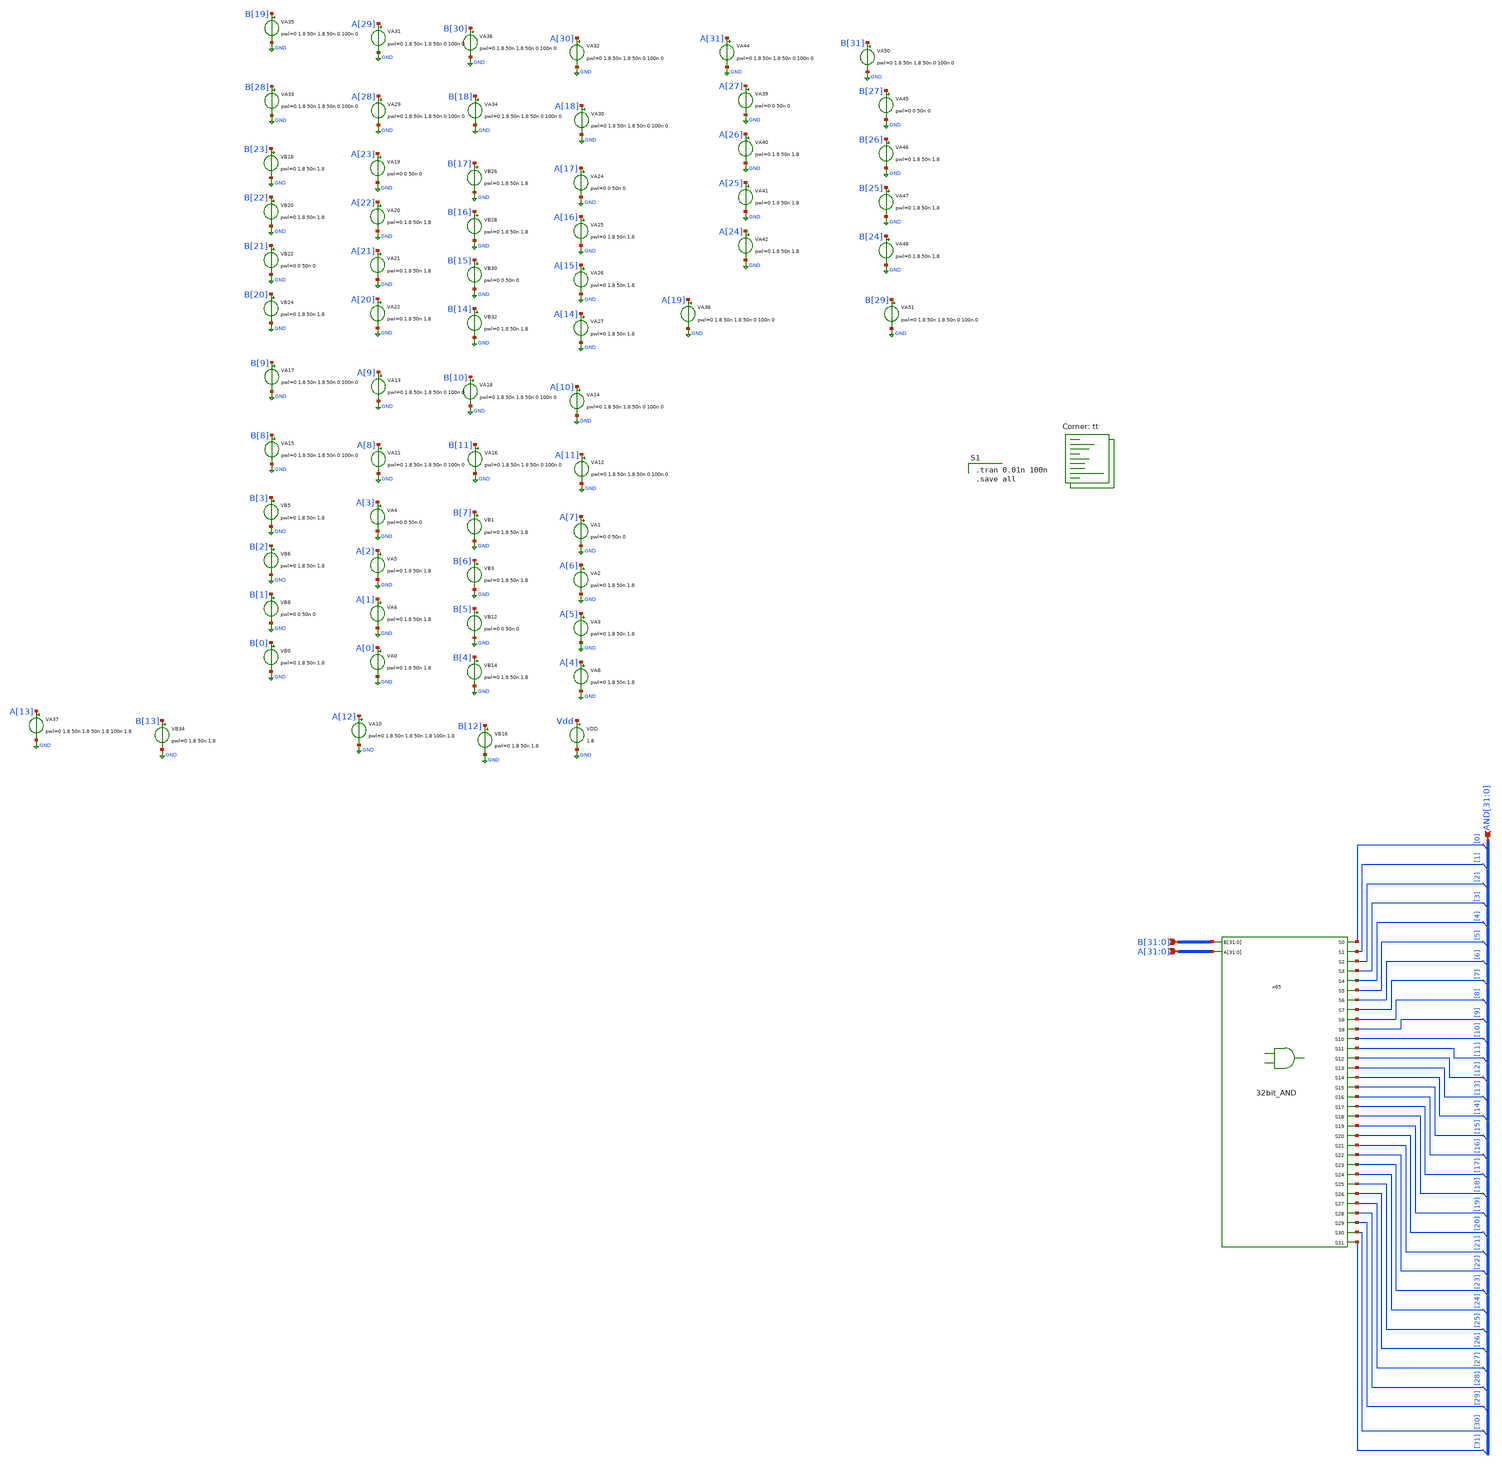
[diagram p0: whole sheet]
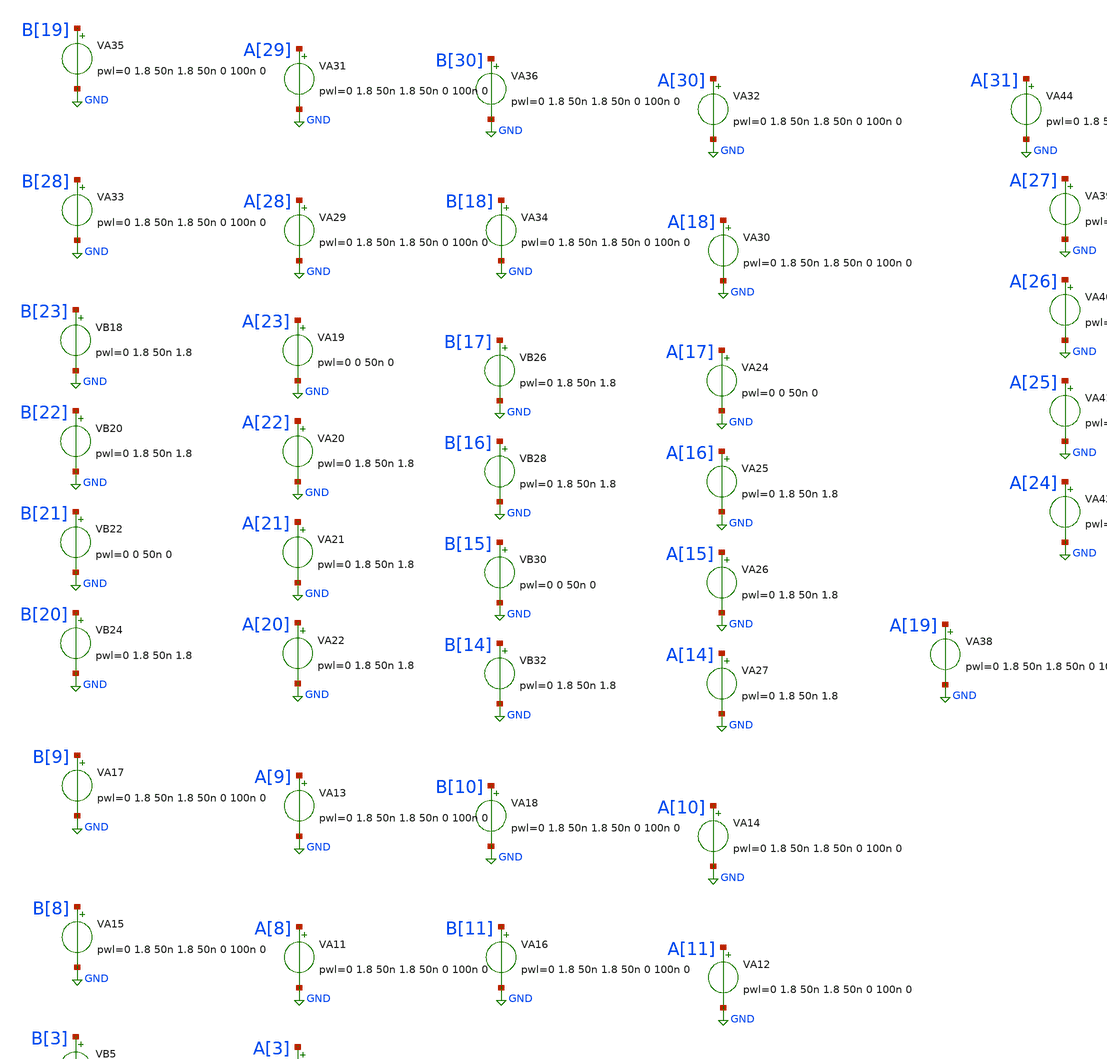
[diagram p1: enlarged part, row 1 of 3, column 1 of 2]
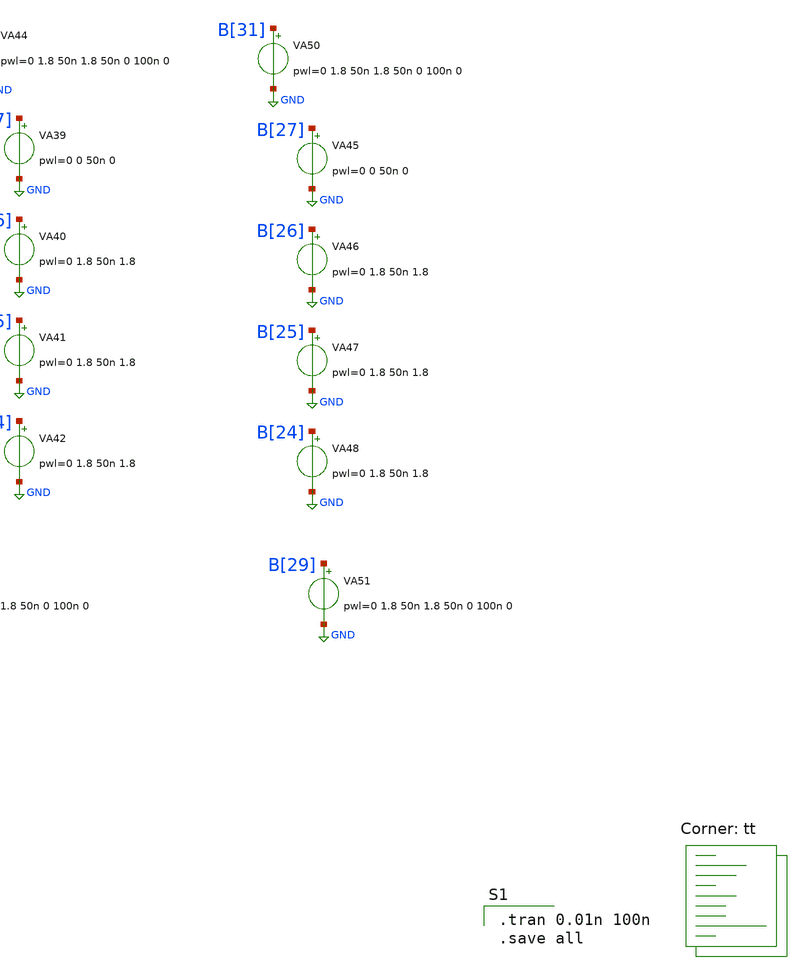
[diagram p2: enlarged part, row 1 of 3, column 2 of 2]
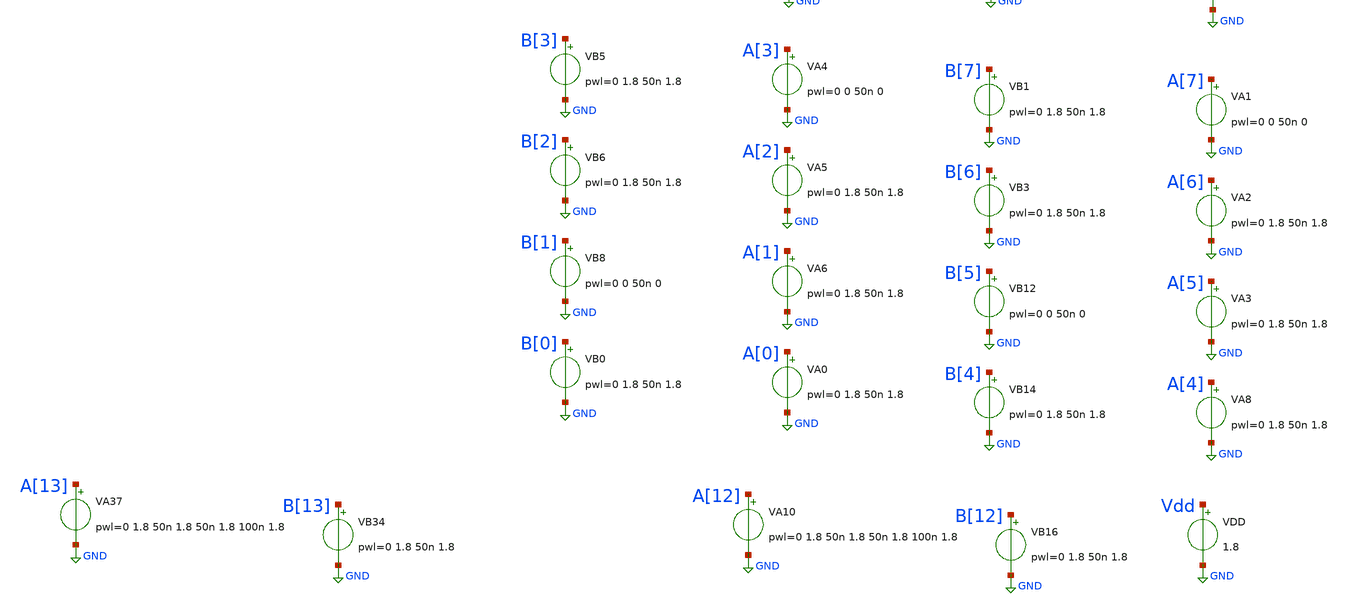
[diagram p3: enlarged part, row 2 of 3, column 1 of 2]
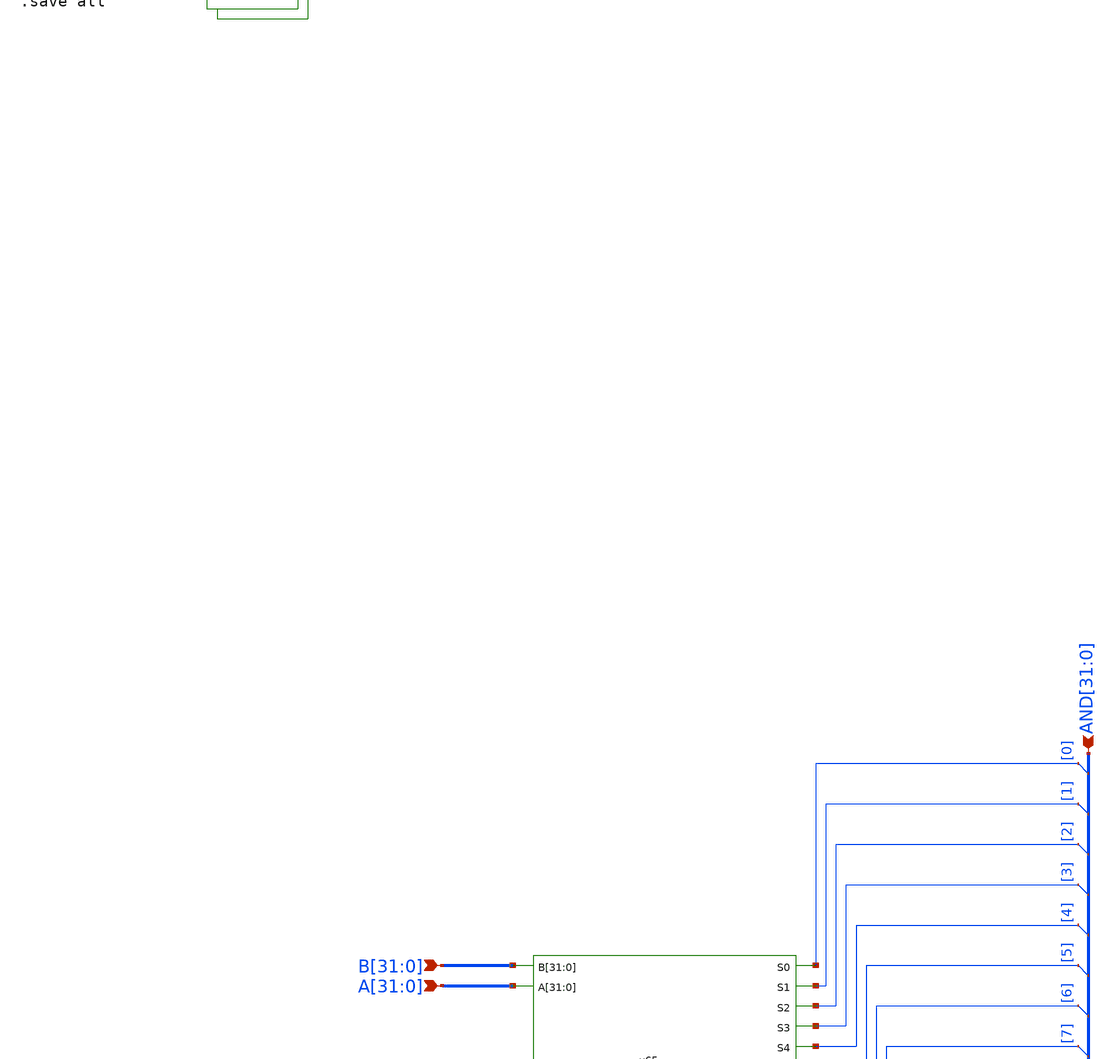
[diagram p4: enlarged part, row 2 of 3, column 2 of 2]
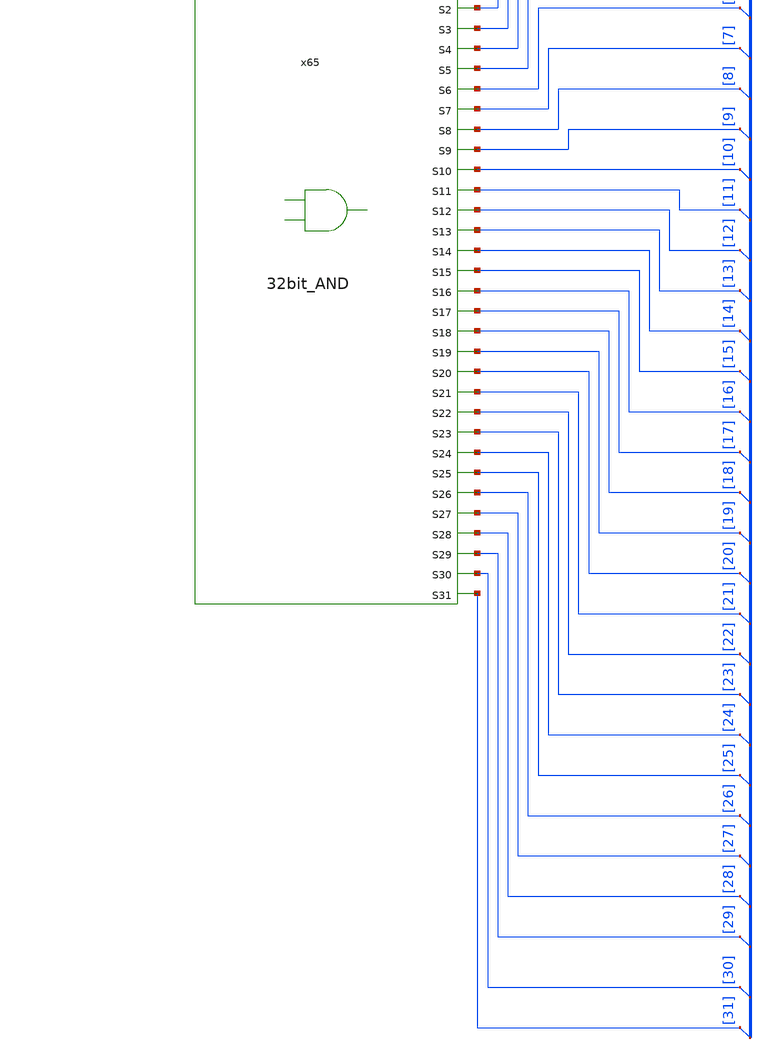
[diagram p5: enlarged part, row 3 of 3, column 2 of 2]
** sch_path: gates/and sym sim.sch
**.subckt and sym sim
*+ AND[31],AND[30],AND[29],AND[28],AND[27],AND[26],AND[25],AND[24],AND[23],AND[22],AND[21],AND[20],AND[19],AND[18],AND[17],AND[16],AND[15],AND[14],AND[13],AND[12],AND[11],AND[10],AND[9],AND[8],AND[7],AND[6],AND[5],AND[4],AND[3],AND[2],AND[1],AND[0]
*+ B[31],B[30],B[29],B[28],B[27],B[26],B[25],B[24],B[23],B[22],B[21],B[20],B[19],B[18],B[17],B[16],B[15],B[14],B[13],B[12],B[11],B[10],B[9],B[8],B[7],B[6],B[5],B[4],B[3],B[2],B[1],B[0]
*+ A[31],A[30],A[29],A[28],A[27],A[26],A[25],A[24],A[23],A[22],A[21],A[20],A[19],A[18],A[17],A[16],A[15],A[14],A[13],A[12],A[11],A[10],A[9],A[8],A[7],A[6],A[5],A[4],A[3],A[2],A[1],A[0]
*.ipin
*+ AND[31],AND[30],AND[29],AND[28],AND[27],AND[26],AND[25],AND[24],AND[23],AND[22],AND[21],AND[20],AND[19],AND[18],AND[17],AND[16],AND[15],AND[14],AND[13],AND[12],AND[11],AND[10],AND[9],AND[8],AND[7],AND[6],AND[5],AND[4],AND[3],AND[2],AND[1],AND[0]
*.ipin
*+ B[31],B[30],B[29],B[28],B[27],B[26],B[25],B[24],B[23],B[22],B[21],B[20],B[19],B[18],B[17],B[16],B[15],B[14],B[13],B[12],B[11],B[10],B[9],B[8],B[7],B[6],B[5],B[4],B[3],B[2],B[1],B[0]
*.ipin
*+ A[31],A[30],A[29],A[28],A[27],A[26],A[25],A[24],A[23],A[22],A[21],A[20],A[19],A[18],A[17],A[16],A[15],A[14],A[13],A[12],A[11],A[10],A[9],A[8],A[7],A[6],A[5],A[4],A[3],A[2],A[1],A[0]
VA10 A[12] GND pwl=0 1.8 50n 1.8 50n 1.8 100n 1.8
VB16 B[12] GND pwl=0 1.8 50n 1.8
VDD Vdd GND 1.8
VA4 A[3] GND pwl=0 0 50n 0
VA5 A[2] GND pwl=0 1.8 50n 1.8
VA6 A[1] GND pwl=0 1.8 50n 1.8
VA0 A[0] GND pwl=0 1.8 50n 1.8
VB5 B[3] GND pwl=0 1.8 50n 1.8
VB6 B[2] GND pwl=0 1.8 50n 1.8
VB8 B[1] GND pwl=0 0 50n 0
VB0 B[0] GND pwl=0 1.8 50n 1.8
VA1 A[7] GND pwl=0 0 50n 0
VA2 A[6] GND pwl=0 1.8 50n 1.8
VA3 A[5] GND pwl=0 1.8 50n 1.8
VA8 A[4] GND pwl=0 1.8 50n 1.8
VB1 B[7] GND pwl=0 1.8 50n 1.8
VB3 B[6] GND pwl=0 1.8 50n 1.8
VB12 B[5] GND pwl=0 0 50n 0
VB14 B[4] GND pwl=0 1.8 50n 1.8
VA11 A[8] GND pwl=0 1.8 50n 1.8 50n 0 100n 0
VA12 A[11] GND pwl=0 1.8 50n 1.8 50n 0 100n 0
VA13 A[9] GND pwl=0 1.8 50n 1.8 50n 0 100n 0
VA14 A[10] GND pwl=0 1.8 50n 1.8 50n 0 100n 0
VA15 B[8] GND pwl=0 1.8 50n 1.8 50n 0 100n 0
VA16 B[11] GND pwl=0 1.8 50n 1.8 50n 0 100n 0
VA17 B[9] GND pwl=0 1.8 50n 1.8 50n 0 100n 0
VA18 B[10] GND pwl=0 1.8 50n 1.8 50n 0 100n 0
VA19 A[23] GND pwl=0 0 50n 0
VA20 A[22] GND pwl=0 1.8 50n 1.8
VA21 A[21] GND pwl=0 1.8 50n 1.8
VA22 A[20] GND pwl=0 1.8 50n 1.8
VB18 B[23] GND pwl=0 1.8 50n 1.8
VB20 B[22] GND pwl=0 1.8 50n 1.8
VB22 B[21] GND pwl=0 0 50n 0
VB24 B[20] GND pwl=0 1.8 50n 1.8
VA24 A[17] GND pwl=0 0 50n 0
VA25 A[16] GND pwl=0 1.8 50n 1.8
VA26 A[15] GND pwl=0 1.8 50n 1.8
VA27 A[14] GND pwl=0 1.8 50n 1.8
VB26 B[17] GND pwl=0 1.8 50n 1.8
VB28 B[16] GND pwl=0 1.8 50n 1.8
VB30 B[15] GND pwl=0 0 50n 0
VB32 B[14] GND pwl=0 1.8 50n 1.8
VA29 A[28] GND pwl=0 1.8 50n 1.8 50n 0 100n 0
VA30 A[18] GND pwl=0 1.8 50n 1.8 50n 0 100n 0
VA31 A[29] GND pwl=0 1.8 50n 1.8 50n 0 100n 0
VA32 A[30] GND pwl=0 1.8 50n 1.8 50n 0 100n 0
VA33 B[28] GND pwl=0 1.8 50n 1.8 50n 0 100n 0
VA34 B[18] GND pwl=0 1.8 50n 1.8 50n 0 100n 0
VA35 B[19] GND pwl=0 1.8 50n 1.8 50n 0 100n 0
VA36 B[30] GND pwl=0 1.8 50n 1.8 50n 0 100n 0
VA37 A[13] GND pwl=0 1.8 50n 1.8 50n 1.8 100n 1.8
VB34 B[13] GND pwl=0 1.8 50n 1.8
VA38 A[19] GND pwl=0 1.8 50n 1.8 50n 0 100n 0
VA39 A[27] GND pwl=0 0 50n 0
VA40 A[26] GND pwl=0 1.8 50n 1.8
VA41 A[25] GND pwl=0 1.8 50n 1.8
VA42 A[24] GND pwl=0 1.8 50n 1.8
VA44 A[31] GND pwl=0 1.8 50n 1.8 50n 0 100n 0
VA45 B[27] GND pwl=0 0 50n 0
VA46 B[26] GND pwl=0 1.8 50n 1.8
VA47 B[25] GND pwl=0 1.8 50n 1.8
VA48 B[24] GND pwl=0 1.8 50n 1.8
VA50 B[31] GND pwl=0 1.8 50n 1.8 50n 0 100n 0
VA51 B[29] GND pwl=0 1.8 50n 1.8 50n 0 100n 0
x65 B[31] B[30] B[29] B[28] B[27] B[26] B[25] B[24] B[23] B[22] B[21] B[20] B[19] B[18] B[17] B[16]
+ B[15] B[14] B[13] B[12] B[11] B[10] B[9] B[8] B[7] B[6] B[5] B[4] B[3] B[2] B[1] B[0] A[31] A[30] A[29]
+ A[28] A[27] A[26] A[25] A[24] A[23] A[22] A[21] A[20] A[19] A[18] A[17] A[16] A[15] A[14] A[13] A[12]
+ A[11] A[10] A[9] A[8] A[7] A[6] A[5] A[4] A[3] A[2] A[1] A[0] AND[0] AND[1] AND[2] AND[3] AND[4] AND[5]
+ AND[6] AND[7] AND[8] AND[9] AND[10] AND[11] AND[12] AND[13] AND[14] AND[15] AND[16] AND[17] AND[18]
+ AND[19] AND[20] AND[21] AND[22] AND[23] AND[24] AND[25] AND[26] AND[27] AND[28] AND[29] AND[30] AND[31]
+ 32bit_AND
* tap: AND[31:0] --> AND[0]
* tap: AND[31:0] --> AND[1]
* tap: AND[31:0] --> AND[2]
* tap: AND[31:0] --> AND[3]
* tap: AND[31:0] --> AND[4]
* tap: AND[31:0] --> AND[5]
* tap: AND[31:0] --> AND[6]
* tap: AND[31:0] --> AND[7]
* tap: AND[31:0] --> AND[8]
* tap: AND[31:0] --> AND[9]
* tap: AND[31:0] --> AND[10]
* tap: AND[31:0] --> AND[11]
* tap: AND[31:0] --> AND[12]
* tap: AND[31:0] --> AND[13]
* tap: AND[31:0] --> AND[14]
* tap: AND[31:0] --> AND[15]
* tap: AND[31:0] --> AND[16]
* tap: AND[31:0] --> AND[17]
* tap: AND[31:0] --> AND[18]
* tap: AND[31:0] --> AND[19]
* tap: AND[31:0] --> AND[20]
* tap: AND[31:0] --> AND[21]
* tap: AND[31:0] --> AND[22]
* tap: AND[31:0] --> AND[23]
* tap: AND[31:0] --> AND[24]
* tap: AND[31:0] --> AND[25]
* tap: AND[31:0] --> AND[26]
* tap: AND[31:0] --> AND[27]
* tap: AND[31:0] --> AND[28]
* tap: AND[31:0] --> AND[29]
* tap: AND[31:0] --> AND[30]
* tap: AND[31:0] --> AND[31]
**** begin user architecture code

.tran 0.01n 100n
.save all

.lib $::SKYWATER_MODELS/sky130.lib.spice tt
**** end user architecture code
**.ends

* expanding   symbol:  /home/apn/test_xschem_sky130/gates/32bit_AND.sym # of pins=34
** sym_path: gates/32bit_AND.sym
** sch_path: gates/32bit_AND.sch
.subckt 32bit_AND B[31] B[30] B[29] B[28] B[27] B[26] B[25] B[24] B[23] B[22] B[21] B[20] B[19]
+ B[18] B[17] B[16] B[15] B[14] B[13] B[12] B[11] B[10] B[9] B[8] B[7] B[6] B[5] B[4] B[3] B[2] B[1] B[0]
+ A[31] A[30] A[29] A[28] A[27] A[26] A[25] A[24] A[23] A[22] A[21] A[20] A[19] A[18] A[17] A[16] A[15]
+ A[14] A[13] A[12] A[11] A[10] A[9] A[8] A[7] A[6] A[5] A[4] A[3] A[2] A[1] A[0] S0 S1 S2 S3 S4 S5 S6 S7
+ S8 S9 S10 S11 S12 S13 S14 S15 S16 S17 S18 S19 S20 S21 S22 S23 S24 S25 S26 S27 S28 S29 S30 S31
*.opin S4
*.opin S5
*.opin S6
*.opin S7
*.opin S8
*.opin S9
*.opin S10
*.opin S11
*.opin S12
*.opin S13
*.opin S14
*.opin S15
*.opin S16
*.opin S17
*.opin S18
*.opin S19
*.opin S20
*.opin S21
*.opin S22
*.opin S23
*.opin S24
*.opin S25
*.opin S26
*.opin S27
*.opin S28
*.opin S29
*.opin S30
*.opin S31
*.opin S0
*.opin S1
*.opin S2
*.opin S3
*.ipin
*+ A[31],A[30],A[29],A[28],A[27],A[26],A[25],A[24],A[23],A[22],A[21],A[20],A[19],A[18],A[17],A[16],A[15],A[14],A[13],A[12],A[11],A[10],A[9],A[8],A[7],A[6],A[5],A[4],A[3],A[2],A[1],A[0]
*.ipin
*+ B[31],B[30],B[29],B[28],B[27],B[26],B[25],B[24],B[23],B[22],B[21],B[20],B[19],B[18],B[17],B[16],B[15],B[14],B[13],B[12],B[11],B[10],B[9],B[8],B[7],B[6],B[5],B[4],B[3],B[2],B[1],B[0]
x0 A[0] S0 B[0] AND2
* tap: A[31:0] --> A[0]
* tap: A[31:0] --> A[1]
* tap: A[31:0] --> A[2]
* tap: A[31:0] --> A[3]
* tap: A[31:0] --> A[4]
* tap: A[31:0] --> A[5]
* tap: A[31:0] --> A[6]
* tap: A[31:0] --> A[7]
* tap: A[31:0] --> A[8]
* tap: A[31:0] --> A[9]
* tap: A[31:0] --> A[10]
* tap: A[31:0] --> A[11]
* tap: A[31:0] --> A[12]
* tap: A[31:0] --> A[13]
* tap: A[31:0] --> A[14]
* tap: A[31:0] --> A[15]
* tap: A[31:0] --> A[16]
* tap: A[31:0] --> A[17]
* tap: A[31:0] --> A[18]
* tap: A[31:0] --> A[19]
* tap: A[31:0] --> A[20]
* tap: A[31:0] --> A[21]
* tap: A[31:0] --> A[22]
* tap: A[31:0] --> A[23]
* tap: A[31:0] --> A[24]
* tap: A[31:0] --> A[25]
* tap: A[31:0] --> A[26]
* tap: A[31:0] --> A[27]
* tap: A[31:0] --> A[28]
* tap: A[31:0] --> A[29]
* tap: A[31:0] --> A[30]
* tap: A[31:0] --> A[31]
* tap: B[31:0] --> B[0]
* tap: B[31:0] --> B[1]
* tap: B[31:0] --> B[2]
* tap: B[31:0] --> B[3]
* tap: B[31:0] --> B[4]
* tap: B[31:0] --> B[5]
* tap: B[31:0] --> B[6]
* tap: B[31:0] --> B[7]
* tap: B[31:0] --> B[8]
* tap: B[31:0] --> B[9]
* tap: B[31:0] --> B[10]
* tap: B[31:0] --> B[11]
* tap: B[31:0] --> B[12]
* tap: B[31:0] --> B[13]
* tap: B[31:0] --> B[14]
* tap: B[31:0] --> B[15]
* tap: B[31:0] --> B[16]
* tap: B[31:0] --> B[17]
* tap: B[31:0] --> B[18]
* tap: B[31:0] --> B[19]
* tap: B[31:0] --> B[20]
* tap: B[31:0] --> B[21]
* tap: B[31:0] --> B[22]
* tap: B[31:0] --> B[23]
* tap: B[31:0] --> B[24]
* tap: B[31:0] --> B[25]
* tap: B[31:0] --> B[26]
* tap: B[31:0] --> B[27]
* tap: B[31:0] --> B[28]
* tap: B[31:0] --> B[29]
* tap: B[31:0] --> B[30]
* tap: B[31:0] --> B[31]
x1 A[1] S1 B[1] AND2
x2 A[2] S2 B[2] AND2
x3 A[3] S3 B[3] AND2
x4 A[4] S4 B[4] AND2
x5 A[5] S5 B[5] AND2
x6 A[6] S6 B[6] AND2
x8 A[8] S8 B[8] AND2
x9 A[9] S9 B[9] AND2
x10 A[10] S10 B[10] AND2
x11 A[11] S11 B[11] AND2
x12 A[12] S12 B[12] AND2
x13 A[13] S13 B[13] AND2
x14 A[14] S14 B[14] AND2
x15 A[15] S15 B[15] AND2
x16 A[16] S16 B[16] AND2
x17 A[17] S17 B[17] AND2
x18 A[18] S18 B[18] AND2
x19 A[19] S19 B[19] AND2
x20 A[20] S20 B[20] AND2
x21 A[21] S21 B[21] AND2
x22 A[22] S22 B[22] AND2
x23 A[23] S23 B[23] AND2
x24 A[24] S24 B[24] AND2
x25 A[25] S25 B[25] AND2
x26 A[26] S26 B[26] AND2
x27 A[27] S27 B[27] AND2
x28 A[28] S28 B[28] AND2
x29 A[29] S29 B[29] AND2
x30 A[30] S30 B[30] AND2
x31 A[31] S31 B[31] AND2
x7 A[7] S7 B[7] AND2
.ends


* expanding   symbol:  AND2.sym # of pins=3
** sym_path: gates/AND2.sym
** sch_path: gates/AND2.sch
.subckt AND2 A Y B
*.opin Y
*.ipin A
*.ipin B
x1 A net1 B NAND2_Gate
X2 net1 Y inv_vtc
.ends


* expanding   symbol:  NAND2_Gate.sym # of pins=3
** sym_path: gates/NAND2_Gate.sym
** sch_path: gates/NAND2_Gate.sch
.subckt NAND2_Gate A Y B
*.ipin A
*.ipin B
*.opin Y
XM1 Y A net1 GND sky130_fd_pr__nfet_01v8 L=0.15 W=1 nf=1 ad='int((nf+1)/2) * W/nf * 0.29' as='int((nf+2)/2) * W/nf * 0.29'
+ pd='2*int((nf+1)/2) * (W/nf + 0.29)' ps='2*int((nf+2)/2) * (W/nf + 0.29)' nrd='0.29 / W' nrs='0.29 / W'
+ sa=0 sb=0 sd=0 mult=1 m=1
XM2 net1 B GND GND sky130_fd_pr__nfet_01v8 L=0.15 W=1 nf=1 ad='int((nf+1)/2) * W/nf * 0.29' as='int((nf+2)/2) * W/nf * 0.29'
+ pd='2*int((nf+1)/2) * (W/nf + 0.29)' ps='2*int((nf+2)/2) * (W/nf + 0.29)' nrd='0.29 / W' nrs='0.29 / W'
+ sa=0 sb=0 sd=0 mult=1 m=1
XM3 Y A VDD VDD sky130_fd_pr__pfet_01v8 L=0.15 W=1 nf=1 ad='int((nf+1)/2) * W/nf * 0.29' as='int((nf+2)/2) * W/nf * 0.29'
+ pd='2*int((nf+1)/2) * (W/nf + 0.29)' ps='2*int((nf+2)/2) * (W/nf + 0.29)' nrd='0.29 / W' nrs='0.29 / W'
+ sa=0 sb=0 sd=0 mult=1 m=1
XM4 Y B VDD VDD sky130_fd_pr__pfet_01v8 L=0.15 W=1 nf=1 ad='int((nf+1)/2) * W/nf * 0.29' as='int((nf+2)/2) * W/nf * 0.29'
+ pd='2*int((nf+1)/2) * (W/nf + 0.29)' ps='2*int((nf+2)/2) * (W/nf + 0.29)' nrd='0.29 / W' nrs='0.29 / W'
+ sa=0 sb=0 sd=0 mult=1 m=1
.ends


* expanding   symbol:  /home/apn/test_xschem_sky130/inv_vtc.sym # of pins=2
** sym_path: gates/inv_vtc.sym
** sch_path: gates/inv_vtc.sch
.subckt inv_vtc A Y
*.ipin A
*.opin Y
XM1 Y A VDD VDD sky130_fd_pr__pfet_01v8 L=0.15 W=2 nf=1 ad='int((nf+1)/2) * W/nf * 0.29' as='int((nf+2)/2) * W/nf * 0.29'
+ pd='2*int((nf+1)/2) * (W/nf + 0.29)' ps='2*int((nf+2)/2) * (W/nf + 0.29)' nrd='0.29 / W' nrs='0.29 / W'
+ sa=0 sb=0 sd=0 mult=1 m=1
XM2 Y A GND GND sky130_fd_pr__nfet_01v8 L=0.15 W=1 nf=1 ad='int((nf+1)/2) * W/nf * 0.29' as='int((nf+2)/2) * W/nf * 0.29'
+ pd='2*int((nf+1)/2) * (W/nf + 0.29)' ps='2*int((nf+2)/2) * (W/nf + 0.29)' nrd='0.29 / W' nrs='0.29 / W'
+ sa=0 sb=0 sd=0 mult=1 m=1
.ends

.GLOBAL GND
.GLOBAL VDD
.end
